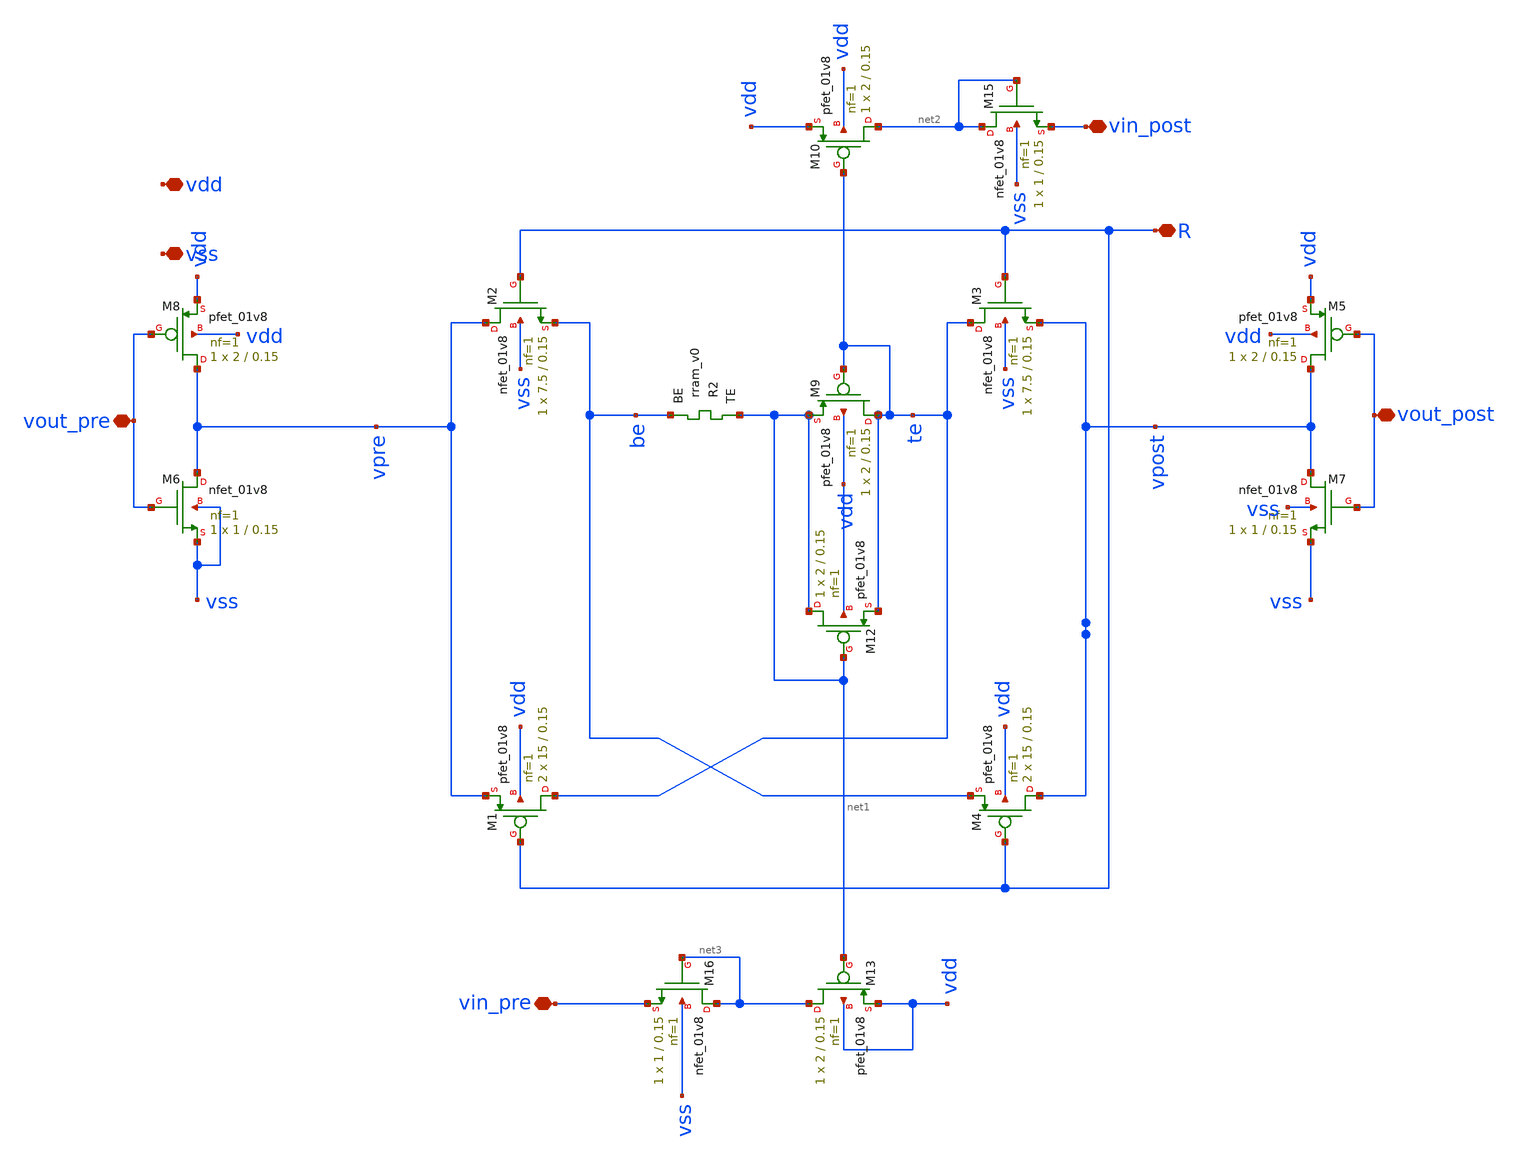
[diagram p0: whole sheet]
** sch_path: Synapse/rstdp_mirror.sch
**.subckt rstdp_mirror vdd vss R vout_post vout_pre vin_post vin_pre
*.iopin vdd
*.iopin vss
*.iopin R
*.iopin vout_post
*.iopin vout_pre
*.iopin vin_post
*.iopin vin_pre
XR2 net1 be rram_v0
XM2 vpre R be vss sky130_fd_pr__nfet_01v8 L=0.15 W=7.5 nf=1 ad='int((nf+1)/2) * W/nf * 0.29' as='int((nf+2)/2) * W/nf * 0.29'
+ pd='2*int((nf+1)/2) * (W/nf + 0.29)' ps='2*int((nf+2)/2) * (W/nf + 0.29)' nrd='0.29 / W' nrs='0.29 / W'
+ sa=0 sb=0 sd=0 mult=1 m=1
XM3 te R vpost vss sky130_fd_pr__nfet_01v8 L=0.15 W=7.5 nf=1 ad='int((nf+1)/2) * W/nf * 0.29' as='int((nf+2)/2) * W/nf * 0.29'
+ pd='2*int((nf+1)/2) * (W/nf + 0.29)' ps='2*int((nf+2)/2) * (W/nf + 0.29)' nrd='0.29 / W' nrs='0.29 / W'
+ sa=0 sb=0 sd=0 mult=1 m=1
XM1 te R vpre vdd sky130_fd_pr__pfet_01v8 L=0.15 W=15 nf=1 ad='int((nf+1)/2) * W/nf * 0.29' as='int((nf+2)/2) * W/nf * 0.29'
+ pd='2*int((nf+1)/2) * (W/nf + 0.29)' ps='2*int((nf+2)/2) * (W/nf + 0.29)' nrd='0.29 / W' nrs='0.29 / W'
+ sa=0 sb=0 sd=0 mult=2 m=2
XM4 vpost R be vdd sky130_fd_pr__pfet_01v8 L=0.15 W=15 nf=1 ad='int((nf+1)/2) * W/nf * 0.29' as='int((nf+2)/2) * W/nf * 0.29'
+ pd='2*int((nf+1)/2) * (W/nf + 0.29)' ps='2*int((nf+2)/2) * (W/nf + 0.29)' nrd='0.29 / W' nrs='0.29 / W'
+ sa=0 sb=0 sd=0 mult=2 m=2
XM7 vpost vout_post vss vss sky130_fd_pr__nfet_01v8 L=0.15 W=1 nf=1 ad='int((1 + 1)/2) * 1 / 1 * 0.29'
+ as='int((1 + 2)/2) * 1 / 1 * 0.29' pd='2*int((1 + 1)/2) * (1 / 1 + 0.29)' ps='2*int((1 + 2)/2) * (1 / 1 + 0.29)'
+ nrd='0.29 / 1 ' nrs='0.29 / 1 ' sa=0 sb=0 sd=0 mult=1 m=1
XM5 vpost vout_post vdd vdd sky130_fd_pr__pfet_01v8 L=0.15 W=2 nf=1 ad='int((nf+1)/2) * W/nf * 0.29'
+ as='int((nf+2)/2) * W/nf * 0.29' pd='2*int((nf+1)/2) * (W/nf + 0.29)' ps='2*int((nf+2)/2) * (W/nf + 0.29)'
+ nrd='0.29 / W' nrs='0.29 / W' sa=0 sb=0 sd=0 mult=1 m=1
XM6 vpre vout_pre vss vss sky130_fd_pr__nfet_01v8 L=0.15 W=1 nf=1 ad='int((1 + 1)/2) * 1 / 1 * 0.29'
+ as='int((1 + 2)/2) * 1 / 1 * 0.29' pd='2*int((1 + 1)/2) * (1 / 1 + 0.29)' ps='2*int((1 + 2)/2) * (1 / 1 + 0.29)'
+ nrd='0.29 / 1 ' nrs='0.29 / 1 ' sa=0 sb=0 sd=0 mult=1 m=1
XM8 vpre vout_pre vdd vdd sky130_fd_pr__pfet_01v8 L=0.15 W=2 nf=1 ad='int((nf+1)/2) * W/nf * 0.29' as='int((nf+2)/2) * W/nf * 0.29'
+ pd='2*int((nf+1)/2) * (W/nf + 0.29)' ps='2*int((nf+2)/2) * (W/nf + 0.29)' nrd='0.29 / W' nrs='0.29 / W'
+ sa=0 sb=0 sd=0 mult=1 m=1
XM9 te te net1 vdd sky130_fd_pr__pfet_01v8 L=0.15 W=2 nf=1 ad='int((nf+1)/2) * W/nf * 0.29' as='int((nf+2)/2) * W/nf * 0.29'
+ pd='2*int((nf+1)/2) * (W/nf + 0.29)' ps='2*int((nf+2)/2) * (W/nf + 0.29)' nrd='0.29 / W' nrs='0.29 / W'
+ sa=0 sb=0 sd=0 mult=1 m=1
XM10 net2 te vdd vdd sky130_fd_pr__pfet_01v8 L=0.15 W=2 nf=1 ad='int((nf+1)/2) * W/nf * 0.29' as='int((nf+2)/2) * W/nf * 0.29'
+ pd='2*int((nf+1)/2) * (W/nf + 0.29)' ps='2*int((nf+2)/2) * (W/nf + 0.29)' nrd='0.29 / W' nrs='0.29 / W'
+ sa=0 sb=0 sd=0 mult=1 m=1
XM12 net1 net1 te vdd sky130_fd_pr__pfet_01v8 L=0.15 W=2 nf=1 ad='int((nf+1)/2) * W/nf * 0.29' as='int((nf+2)/2) * W/nf * 0.29'
+ pd='2*int((nf+1)/2) * (W/nf + 0.29)' ps='2*int((nf+2)/2) * (W/nf + 0.29)' nrd='0.29 / W' nrs='0.29 / W'
+ sa=0 sb=0 sd=0 mult=1 m=1
XM13 net3 net1 vdd vdd sky130_fd_pr__pfet_01v8 L=0.15 W=2 nf=1 ad='int((nf+1)/2) * W/nf * 0.29' as='int((nf+2)/2) * W/nf * 0.29'
+ pd='2*int((nf+1)/2) * (W/nf + 0.29)' ps='2*int((nf+2)/2) * (W/nf + 0.29)' nrd='0.29 / W' nrs='0.29 / W'
+ sa=0 sb=0 sd=0 mult=1 m=1
XM15 net2 net2 vin_post vss sky130_fd_pr__nfet_01v8 L=0.15 W=1 nf=1 ad='int((nf+1)/2) * W/nf * 0.29'
+ as='int((nf+2)/2) * W/nf * 0.29' pd='2*int((nf+1)/2) * (W/nf + 0.29)' ps='2*int((nf+2)/2) * (W/nf + 0.29)'
+ nrd='0.29 / W' nrs='0.29 / W' sa=0 sb=0 sd=0 mult=1 m=1
XM16 net3 net3 vin_pre vss sky130_fd_pr__nfet_01v8 L=0.15 W=1 nf=1 ad='int((nf+1)/2) * W/nf * 0.29' as='int((nf+2)/2) * W/nf * 0.29'
+ pd='2*int((nf+1)/2) * (W/nf + 0.29)' ps='2*int((nf+2)/2) * (W/nf + 0.29)' nrd='0.29 / W' nrs='0.29 / W'
+ sa=0 sb=0 sd=0 mult=1 m=1
**.ends
.end
